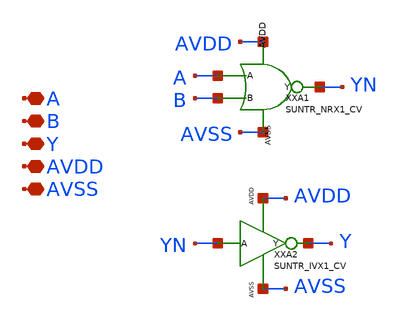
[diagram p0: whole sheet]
** sch_path: ip/sun_tr_sky130nm/design/SUN_TR_SKY130NM/SUNTR_ORX4_CV.sch
**.subckt SUNTR_ORX4_CV A B Y AVDD AVSS
*.iopin A
*.iopin B
*.iopin Y
*.iopin AVDD
*.iopin AVSS
XXA1 YN B AVSS AVDD A SUNTR_NRX1_CV
XXA2 YN Y AVDD AVSS SUNTR_IVX1_CV
**.ends
.end
